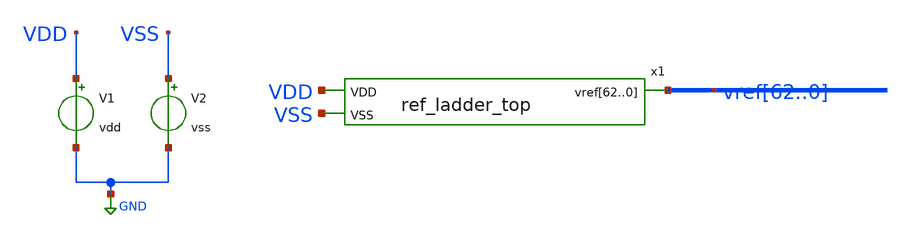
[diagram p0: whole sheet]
** sch_path: simulation/tb_ref_ladder_top.sch
**.subckt tb_ref_ladder_top
V1 VDD GND vdd
V2 VSS GND vss
x1 VDD vref62 vref61 vref60 vref59 vref58 vref57 vref56 vref55 vref54 vref53 vref52 vref51 vref50
+ vref49 vref48 vref47 vref46 vref45 vref44 vref43 vref42 vref41 vref40 vref39 vref38 vref37 vref36 vref35
+ vref34 vref33 vref32 vref31 vref30 vref29 vref28 vref27 vref26 vref25 vref24 vref23 vref22 vref21 vref20
+ vref19 vref18 vref17 vref16 vref15 vref14 vref13 vref12 vref11 vref10 vref9 vref8 vref7 vref6 vref5 vref4
+ vref3 vref2 vref1 vref0 VSS ref_ladder_top
**** begin user architecture code


.lib /usr/local/share/pdk/sky130A/libs.tech/ngspice/sky130.lib.spice tt

.param vdd=1.8 vss=0
.op
.save VDD VSS vref0 vref1 vref2 vref3 vref4 vref5 vref6 vref7 vref8 vref9 vref10 vref11 vref12 vref13 vref14 vref15 vref16 vref17 vref18 vref19 vref20 vref21 vref22 vref23 vref24 vref25 vref26 vref27 vref28 vref29 vref30 vref31 vref32 vref33 vref34 vref35 vref36 vref37 vref38 vref39 vref40 vref41 vref42 vref43 vref44 vref45 vref46 vref47 vref48 vref49 vref50 vref51 vref52 vref53 vref54 vref55 vref56 vref57 vref58 vref59 vref60 vref61 vref62


.control

run
wrdata data.txt vref0 vref1 vref2 vref3 vref4 vref5 vref6 vref7 vref8 vref9 vref10 vref11 vref12
+ vref13 vref14 vref15 vref16 vref17 vref18 vref19 vref20 vref21 vref22 vref23 vref24 vref25 vref26 vref27
+ vref28 vref29 vref30 vref31 vref32 vref33 vref34 vref35 vref36 vref37 vref38 vref39 vref40 vref41 vref42
+ vref43 vref44 vref45 vref46 vref47 vref48 vref49 vref50 vref51 vref52 vref53 vref54 vref55 vref56 vref57
+ vref58 vref59 vref60 vref61 vref62


.endc












**** end user architecture code
**.ends
.GLOBAL GND
.end
